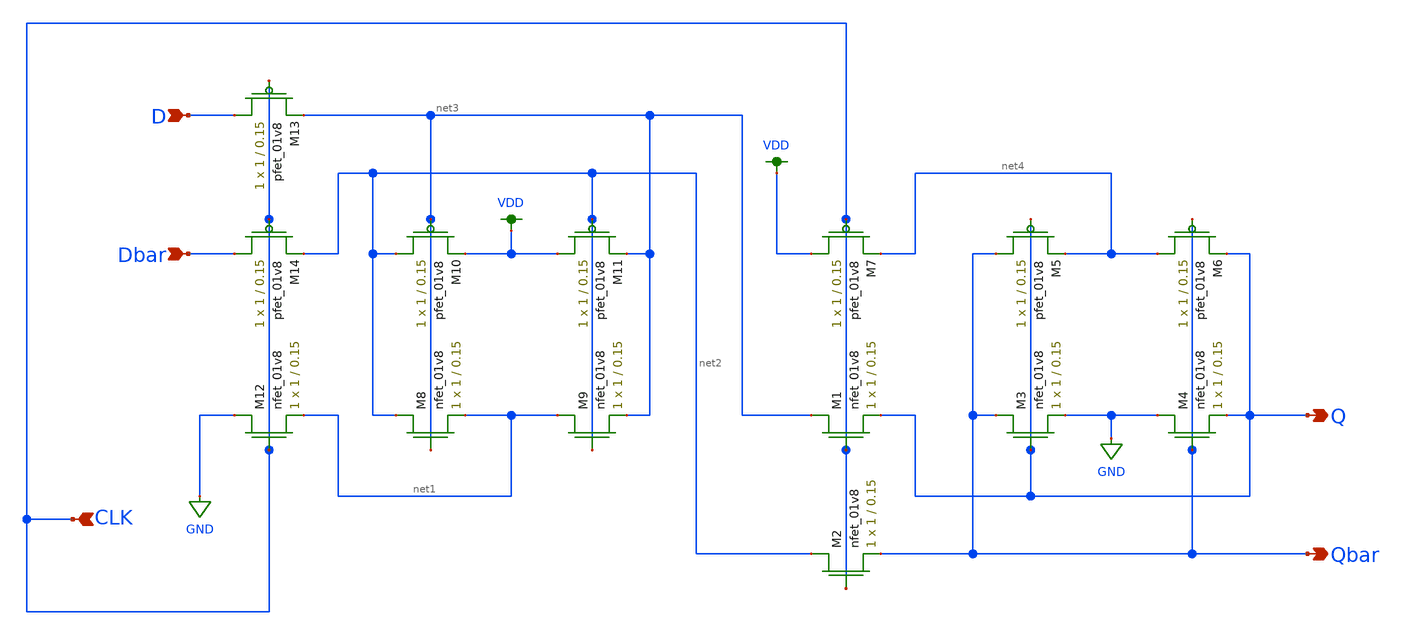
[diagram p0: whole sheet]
** sch_path: mp2/xschem/flipflop/lvs/flipflop_layout_lvs.sch
**.subckt flipflop_layout_lvs D Dbar Q Qbar CLK
*.ipin D
*.ipin Dbar
*.opin Q
*.opin Qbar
*.ipin CLK
XM1 net3 CLK Q GND sky130_fd_pr__nfet_01v8 L=0.15 W=1 nf=1 ad='int((nf+1)/2) * W/nf * 0.29' as='int((nf+2)/2) * W/nf * 0.29'
+ pd='2*int((nf+1)/2) * (W/nf + 0.29)' ps='2*int((nf+2)/2) * (W/nf + 0.29)' nrd='0.29 / W' nrs='0.29 / W'
+ sa=0 sb=0 sd=0 mult=1 m=1
XM2 net2 CLK Qbar GND sky130_fd_pr__nfet_01v8 L=0.15 W=1 nf=1 ad='int((nf+1)/2) * W/nf * 0.29' as='int((nf+2)/2) * W/nf * 0.29'
+ pd='2*int((nf+1)/2) * (W/nf + 0.29)' ps='2*int((nf+2)/2) * (W/nf + 0.29)' nrd='0.29 / W' nrs='0.29 / W'
+ sa=0 sb=0 sd=0 mult=1 m=1
XM3 Qbar Q GND GND sky130_fd_pr__nfet_01v8 L=0.15 W=1 nf=1 ad='int((nf+1)/2) * W/nf * 0.29' as='int((nf+2)/2) * W/nf * 0.29'
+ pd='2*int((nf+1)/2) * (W/nf + 0.29)' ps='2*int((nf+2)/2) * (W/nf + 0.29)' nrd='0.29 / W' nrs='0.29 / W'
+ sa=0 sb=0 sd=0 mult=1 m=1
XM4 GND Qbar Q GND sky130_fd_pr__nfet_01v8 L=0.15 W=1 nf=1 ad='int((nf+1)/2) * W/nf * 0.29' as='int((nf+2)/2) * W/nf * 0.29'
+ pd='2*int((nf+1)/2) * (W/nf + 0.29)' ps='2*int((nf+2)/2) * (W/nf + 0.29)' nrd='0.29 / W' nrs='0.29 / W'
+ sa=0 sb=0 sd=0 mult=1 m=1
XM5 Qbar Q net4 VDD sky130_fd_pr__pfet_01v8 L=0.15 W=1 nf=1 ad='int((nf+1)/2) * W/nf * 0.29' as='int((nf+2)/2) * W/nf * 0.29'
+ pd='2*int((nf+1)/2) * (W/nf + 0.29)' ps='2*int((nf+2)/2) * (W/nf + 0.29)' nrd='0.29 / W' nrs='0.29 / W'
+ sa=0 sb=0 sd=0 mult=1 m=1
XM6 net4 Qbar Q VDD sky130_fd_pr__pfet_01v8 L=0.15 W=1 nf=1 ad='int((nf+1)/2) * W/nf * 0.29' as='int((nf+2)/2) * W/nf * 0.29'
+ pd='2*int((nf+1)/2) * (W/nf + 0.29)' ps='2*int((nf+2)/2) * (W/nf + 0.29)' nrd='0.29 / W' nrs='0.29 / W'
+ sa=0 sb=0 sd=0 mult=1 m=1
XM7 VDD CLK net4 VDD sky130_fd_pr__pfet_01v8 L=0.15 W=1 nf=1 ad='int((nf+1)/2) * W/nf * 0.29' as='int((nf+2)/2) * W/nf * 0.29'
+ pd='2*int((nf+1)/2) * (W/nf + 0.29)' ps='2*int((nf+2)/2) * (W/nf + 0.29)' nrd='0.29 / W' nrs='0.29 / W'
+ sa=0 sb=0 sd=0 mult=1 m=1
XM8 net2 net3 net1 GND sky130_fd_pr__nfet_01v8 L=0.15 W=1 nf=1 ad='int((nf+1)/2) * W/nf * 0.29' as='int((nf+2)/2) * W/nf * 0.29'
+ pd='2*int((nf+1)/2) * (W/nf + 0.29)' ps='2*int((nf+2)/2) * (W/nf + 0.29)' nrd='0.29 / W' nrs='0.29 / W'
+ sa=0 sb=0 sd=0 mult=1 m=1
XM9 net1 net2 net3 GND sky130_fd_pr__nfet_01v8 L=0.15 W=1 nf=1 ad='int((nf+1)/2) * W/nf * 0.29' as='int((nf+2)/2) * W/nf * 0.29'
+ pd='2*int((nf+1)/2) * (W/nf + 0.29)' ps='2*int((nf+2)/2) * (W/nf + 0.29)' nrd='0.29 / W' nrs='0.29 / W'
+ sa=0 sb=0 sd=0 mult=1 m=1
XM10 net2 net3 VDD VDD sky130_fd_pr__pfet_01v8 L=0.15 W=1 nf=1 ad='int((nf+1)/2) * W/nf * 0.29' as='int((nf+2)/2) * W/nf * 0.29'
+ pd='2*int((nf+1)/2) * (W/nf + 0.29)' ps='2*int((nf+2)/2) * (W/nf + 0.29)' nrd='0.29 / W' nrs='0.29 / W'
+ sa=0 sb=0 sd=0 mult=1 m=1
XM11 VDD net2 net3 VDD sky130_fd_pr__pfet_01v8 L=0.15 W=1 nf=1 ad='int((nf+1)/2) * W/nf * 0.29' as='int((nf+2)/2) * W/nf * 0.29'
+ pd='2*int((nf+1)/2) * (W/nf + 0.29)' ps='2*int((nf+2)/2) * (W/nf + 0.29)' nrd='0.29 / W' nrs='0.29 / W'
+ sa=0 sb=0 sd=0 mult=1 m=1
XM12 GND CLK net1 GND sky130_fd_pr__nfet_01v8 L=0.15 W=1 nf=1 ad='int((nf+1)/2) * W/nf * 0.29' as='int((nf+2)/2) * W/nf * 0.29'
+ pd='2*int((nf+1)/2) * (W/nf + 0.29)' ps='2*int((nf+2)/2) * (W/nf + 0.29)' nrd='0.29 / W' nrs='0.29 / W'
+ sa=0 sb=0 sd=0 mult=1 m=1
XM13 D CLK net3 VDD sky130_fd_pr__pfet_01v8 L=0.15 W=1 nf=1 ad='int((nf+1)/2) * W/nf * 0.29' as='int((nf+2)/2) * W/nf * 0.29'
+ pd='2*int((nf+1)/2) * (W/nf + 0.29)' ps='2*int((nf+2)/2) * (W/nf + 0.29)' nrd='0.29 / W' nrs='0.29 / W'
+ sa=0 sb=0 sd=0 mult=1 m=1
XM14 Dbar CLK net2 VDD sky130_fd_pr__pfet_01v8 L=0.15 W=1 nf=1 ad='int((nf+1)/2) * W/nf * 0.29' as='int((nf+2)/2) * W/nf * 0.29'
+ pd='2*int((nf+1)/2) * (W/nf + 0.29)' ps='2*int((nf+2)/2) * (W/nf + 0.29)' nrd='0.29 / W' nrs='0.29 / W'
+ sa=0 sb=0 sd=0 mult=1 m=1
**.ends
.GLOBAL GND
.GLOBAL VDD
.end
